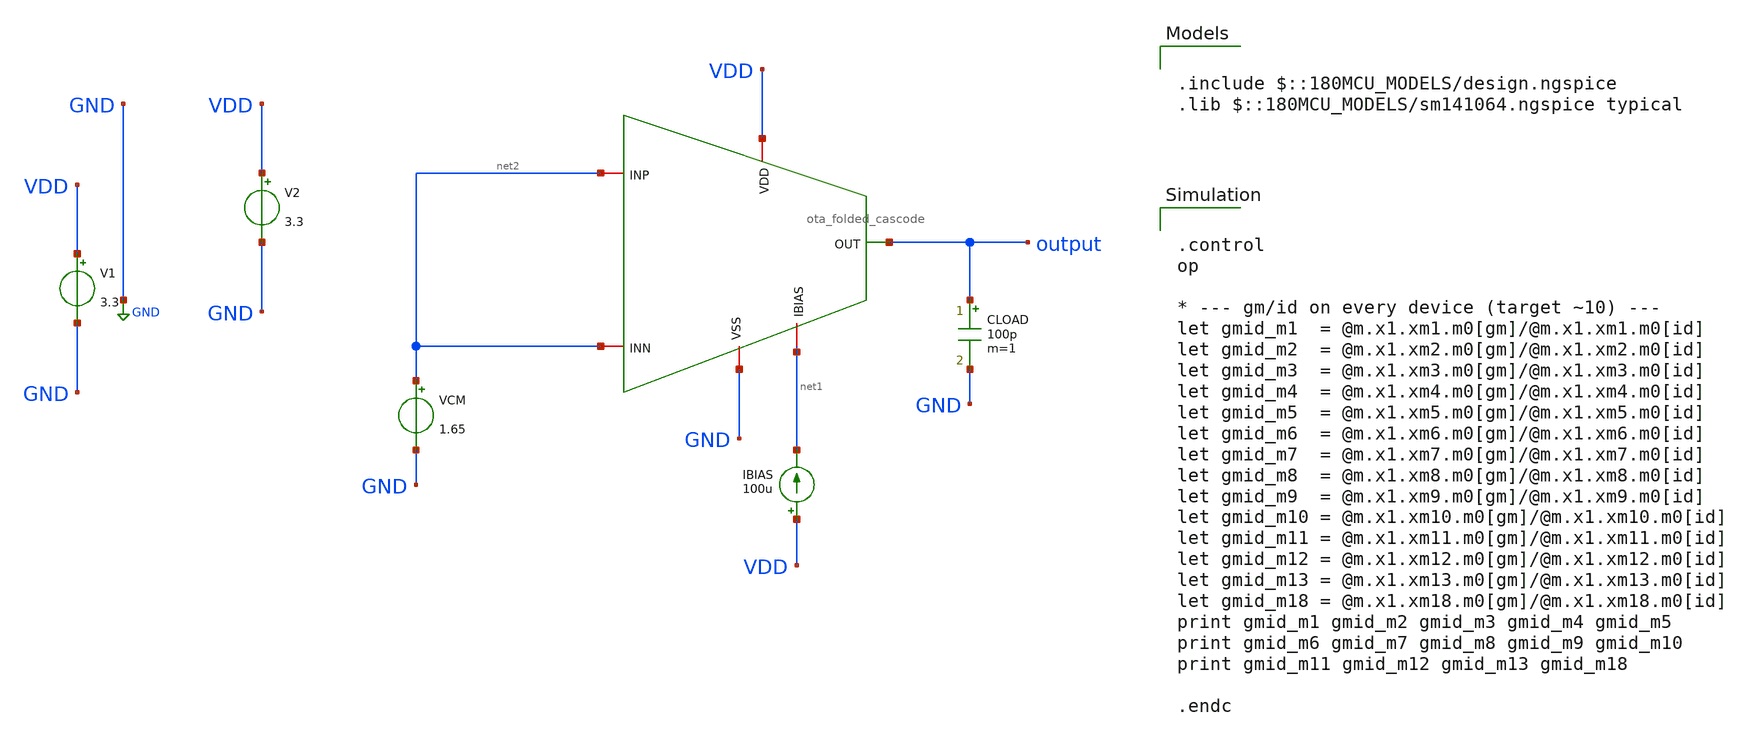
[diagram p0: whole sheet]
** sch_path: designs/libs/core_amps/ota_folded_cascode/op_gmid_tb.sch
**.subckt op_gmid_tb
IBIAS VDD net1 100u
V2 VDD GND 3.3
CLOAD output GND 100p m=1
VCM net2 GND 1.65
x1 VDD GND output net2 net2 net1 ota_folded_cascode
V1 VDD GND 3.3
**** begin user architecture code

.include $::180MCU_MODELS/design.ngspice
.lib $::180MCU_MODELS/sm141064.ngspice typical



.control
op

* --- gm/id on every device (target ~10) ---
let gmid_m1  = @m.x1.xm1.m0[gm]/@m.x1.xm1.m0[id]
let gmid_m2  = @m.x1.xm2.m0[gm]/@m.x1.xm2.m0[id]
let gmid_m3  = @m.x1.xm3.m0[gm]/@m.x1.xm3.m0[id]
let gmid_m4  = @m.x1.xm4.m0[gm]/@m.x1.xm4.m0[id]
let gmid_m5  = @m.x1.xm5.m0[gm]/@m.x1.xm5.m0[id]
let gmid_m6  = @m.x1.xm6.m0[gm]/@m.x1.xm6.m0[id]
let gmid_m7  = @m.x1.xm7.m0[gm]/@m.x1.xm7.m0[id]
let gmid_m8  = @m.x1.xm8.m0[gm]/@m.x1.xm8.m0[id]
let gmid_m9  = @m.x1.xm9.m0[gm]/@m.x1.xm9.m0[id]
let gmid_m10 = @m.x1.xm10.m0[gm]/@m.x1.xm10.m0[id]
let gmid_m11 = @m.x1.xm11.m0[gm]/@m.x1.xm11.m0[id]
let gmid_m12 = @m.x1.xm12.m0[gm]/@m.x1.xm12.m0[id]
let gmid_m13 = @m.x1.xm13.m0[gm]/@m.x1.xm13.m0[id]
let gmid_m18 = @m.x1.xm18.m0[gm]/@m.x1.xm18.m0[id]
print gmid_m1 gmid_m2 gmid_m3 gmid_m4 gmid_m5
print gmid_m6 gmid_m7 gmid_m8 gmid_m9 gmid_m10
print gmid_m11 gmid_m12 gmid_m13 gmid_m18

.endc


**** end user architecture code
**.ends
.GLOBAL GND
.end
